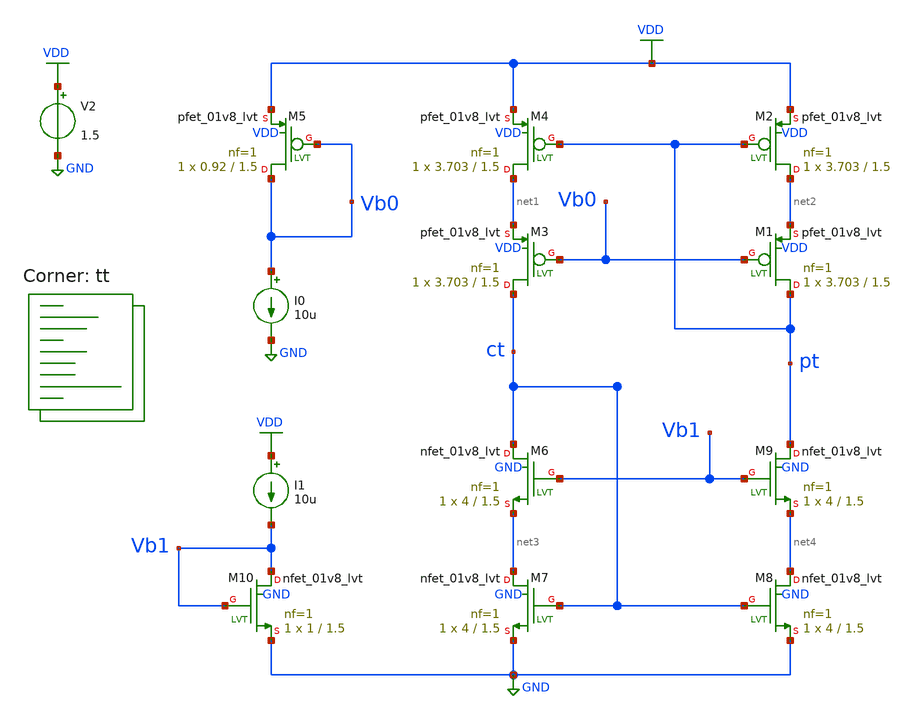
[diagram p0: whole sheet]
** sch_path: Schematic Files/Curr-mirr-test.sch
**.subckt Curr-mirr-test
XM4 net1 pt VDD VDD sky130_fd_pr__pfet_01v8_lvt L=1.5 W=3.703 nf=1 ad='int((nf+1)/2) * W/nf * 0.29' as='int((nf+2)/2) * W/nf * 0.29'
+ pd='2*int((nf+1)/2) * (W/nf + 0.29)' ps='2*int((nf+2)/2) * (W/nf + 0.29)' nrd='0.29 / W' nrs='0.29 / W'
+ sa=0 sb=0 sd=0 mult=1 m=1
V2 VDD GND 1.5
XM5 Vb0 Vb0 VDD VDD sky130_fd_pr__pfet_01v8_lvt L=1.5 W=0.92 nf=1 ad='int((nf+1)/2) * W/nf * 0.29' as='int((nf+2)/2) * W/nf * 0.29'
+ pd='2*int((nf+1)/2) * (W/nf + 0.29)' ps='2*int((nf+2)/2) * (W/nf + 0.29)' nrd='0.29 / W' nrs='0.29 / W'
+ sa=0 sb=0 sd=0 mult=1 m=1
I0 Vb0 GND 10u
XM1 pt Vb0 net2 VDD sky130_fd_pr__pfet_01v8_lvt L=1.5 W=3.703 nf=1 ad='int((nf+1)/2) * W/nf * 0.29' as='int((nf+2)/2) * W/nf * 0.29'
+ pd='2*int((nf+1)/2) * (W/nf + 0.29)' ps='2*int((nf+2)/2) * (W/nf + 0.29)' nrd='0.29 / W' nrs='0.29 / W'
+ sa=0 sb=0 sd=0 mult=1 m=1
XM2 net2 pt VDD VDD sky130_fd_pr__pfet_01v8_lvt L=1.5 W=3.703 nf=1 ad='int((nf+1)/2) * W/nf * 0.29' as='int((nf+2)/2) * W/nf * 0.29'
+ pd='2*int((nf+1)/2) * (W/nf + 0.29)' ps='2*int((nf+2)/2) * (W/nf + 0.29)' nrd='0.29 / W' nrs='0.29 / W'
+ sa=0 sb=0 sd=0 mult=1 m=1
XM3 ct Vb0 net1 VDD sky130_fd_pr__pfet_01v8_lvt L=1.5 W=3.703 nf=1 ad='int((nf+1)/2) * W/nf * 0.29' as='int((nf+2)/2) * W/nf * 0.29'
+ pd='2*int((nf+1)/2) * (W/nf + 0.29)' ps='2*int((nf+2)/2) * (W/nf + 0.29)' nrd='0.29 / W' nrs='0.29 / W'
+ sa=0 sb=0 sd=0 mult=1 m=1
XM6 ct Vb1 net3 GND sky130_fd_pr__nfet_01v8_lvt L=1.5 W=4 nf=1 ad='int((nf+1)/2) * W/nf * 0.29' as='int((nf+2)/2) * W/nf * 0.29'
+ pd='2*int((nf+1)/2) * (W/nf + 0.29)' ps='2*int((nf+2)/2) * (W/nf + 0.29)' nrd='0.29 / W' nrs='0.29 / W'
+ sa=0 sb=0 sd=0 mult=1 m=1
I1 VDD Vb1 10u
XM7 net3 ct GND GND sky130_fd_pr__nfet_01v8_lvt L=1.5 W=4 nf=1 ad='int((nf+1)/2) * W/nf * 0.29' as='int((nf+2)/2) * W/nf * 0.29'
+ pd='2*int((nf+1)/2) * (W/nf + 0.29)' ps='2*int((nf+2)/2) * (W/nf + 0.29)' nrd='0.29 / W' nrs='0.29 / W'
+ sa=0 sb=0 sd=0 mult=1 m=1
XM8 net4 ct GND GND sky130_fd_pr__nfet_01v8_lvt L=1.5 W=4 nf=1 ad='int((nf+1)/2) * W/nf * 0.29' as='int((nf+2)/2) * W/nf * 0.29'
+ pd='2*int((nf+1)/2) * (W/nf + 0.29)' ps='2*int((nf+2)/2) * (W/nf + 0.29)' nrd='0.29 / W' nrs='0.29 / W'
+ sa=0 sb=0 sd=0 mult=1 m=1
XM9 pt Vb1 net4 GND sky130_fd_pr__nfet_01v8_lvt L=1.5 W=4 nf=1 ad='int((nf+1)/2) * W/nf * 0.29' as='int((nf+2)/2) * W/nf * 0.29'
+ pd='2*int((nf+1)/2) * (W/nf + 0.29)' ps='2*int((nf+2)/2) * (W/nf + 0.29)' nrd='0.29 / W' nrs='0.29 / W'
+ sa=0 sb=0 sd=0 mult=1 m=1
XM10 Vb1 Vb1 GND GND sky130_fd_pr__nfet_01v8_lvt L=1.5 W=1 nf=1 ad='int((nf+1)/2) * W/nf * 0.29' as='int((nf+2)/2) * W/nf * 0.29'
+ pd='2*int((nf+1)/2) * (W/nf + 0.29)' ps='2*int((nf+2)/2) * (W/nf + 0.29)' nrd='0.29 / W' nrs='0.29 / W'
+ sa=0 sb=0 sd=0 mult=1 m=1
**** begin user architecture code
.lib $::SKYWATER_MODELS/sky130.lib.spice tt


.option wnflag=1
.option savecurrents
.temp 25 **You can vary the temperature at which you calculate your Operating point
.control
save all
write  Curr-mirr-test.raw
set appendwrite
save @m.xm1.msky130_fd_pr__pfet_01v8_lvt[gm]
save @m.xm2.msky130_fd_pr__pfet_01v8_lvt[gm]
save @m.xm3.msky130_fd_pr__pfet_01v8_lvt[gm]
save @m.xm4.msky130_fd_pr__pfet_01v8_lvt[gm]
save @m.xm5.msky130_fd_pr__pfet_01v8_lvt[gm]
save @m.xm1.msky130_fd_pr__pfet_01v8_lvt[id]
save @m.xm2.msky130_fd_pr__pfet_01v8_lvt[id]
save @m.xm3.msky130_fd_pr__pfet_01v8_lvt[id]
save @m.xm4.msky130_fd_pr__pfet_01v8_lvt[id]
save @m.xm5.msky130_fd_pr__pfet_01v8_lvt[id]
save @m.xm1.msky130_fd_pr__pfet_01v8_lvt[cgg]
save @m.xm2.msky130_fd_pr__pfet_01v8_lvt[cgg]
save @m.xm3.msky130_fd_pr__pfet_01v8_lvt[cgg]
save @m.xm4.msky130_fd_pr__pfet_01v8_lvt[cgg]
save @m.xm5.msky130_fd_pr__pfet_01v8_lvt[cgg]
save @m.xm1.msky130_fd_pr__pfet_01v8_lvt[cgs]
save @m.xm2.msky130_fd_pr__pfet_01v8_lvt[cgs]
save @m.xm3.msky130_fd_pr__pfet_01v8_lvt[cgs]
save @m.xm4.msky130_fd_pr__pfet_01v8_lvt[cgs]
save @m.xm5.msky130_fd_pr__pfet_01v8_lvt[cgs]
save @m.xm6.msky130_fd_pr__nfet_01v8_lvt[gm]
save @m.xm7.msky130_fd_pr__nfet_01v8_lvt[gm]
save @m.xm8.msky130_fd_pr__nfet_01v8_lvt[gm]
save @m.xm9.msky130_fd_pr__nfet_01v8_lvt[gm]
save @m.xm10.msky130_fd_pr__nfet_01v8_lvt[gm]
save @m.xm6.msky130_fd_pr__nfet_01v8_lvt[id]
save @m.xm7.msky130_fd_pr__nfet_01v8_lvt[id]
save @m.xm8.msky130_fd_pr__nfet_01v8_lvt[id]
save @m.xm9.msky130_fd_pr__nfet_01v8_lvt[id]
save @m.xm10.msky130_fd_pr__nfet_01v8_lvt[id]
save @m.xm1.msky130_fd_pr__nfet_01v8_lvt[cgg]
save @m.xm2.msky130_fd_pr__nfet_01v8_lvt[cgg]
save @m.xm3.msky130_fd_pr__nfet_01v8_lvt[cgg]
save @m.xm4.msky130_fd_pr__nfet_01v8_lvt[cgg]
save @m.xm5.msky130_fd_pr__nfet_01v8_lvt[cgg]
save @m.xm1.msky130_fd_pr__nfet_01v8_lvt[cgs]
save @m.xm2.msky130_fd_pr__nfet_01v8_lvt[cgs]
save @m.xm3.msky130_fd_pr__nfet_01v8_lvt[cgs]
save @m.xm4.msky130_fd_pr__nfet_01v8_lvt[cgs]
save @m.xm5.msky130_fd_pr__nfet_01v8_lvt[cgs]
op
write Curr-mirr-test.raw
** ac dec 20 1 1e8
dc V2 1.5 3.3 1m
**tran 1m 100m 1m
.endc

**** end user architecture code
**.ends
.GLOBAL VDD
.GLOBAL GND
.end
